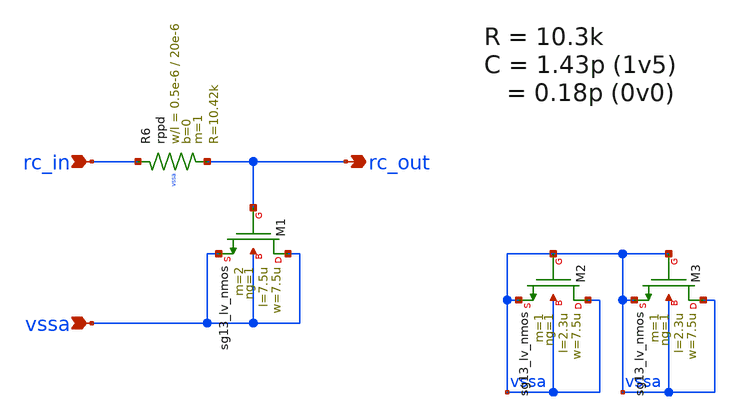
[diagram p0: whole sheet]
** sch_path: Schematics_Layout/sunrise_ro_rc/sunrise_ro_rc.sch
**.subckt sunrise_ro_rc rc_in rc_out vssa
*.ipin rc_in
*.opin rc_out
*.ipin vssa
XM1 vssa rc_out vssa vssa sg13_lv_nmos w=7.5u l=7.5u ng=1 m=2 mm_ok=1
XR6 rc_in rc_out vssa rppd w=0.5e-6 l=20e-6 m=1 b=0 mm_ok=1
XM2 vssa vssa vssa vssa sg13_lv_nmos w=7.5u l=2.3u ng=1 m=1 mm_ok=1
XM3 vssa vssa vssa vssa sg13_lv_nmos w=7.5u l=2.3u ng=1 m=1 mm_ok=1
**.ends
.end
